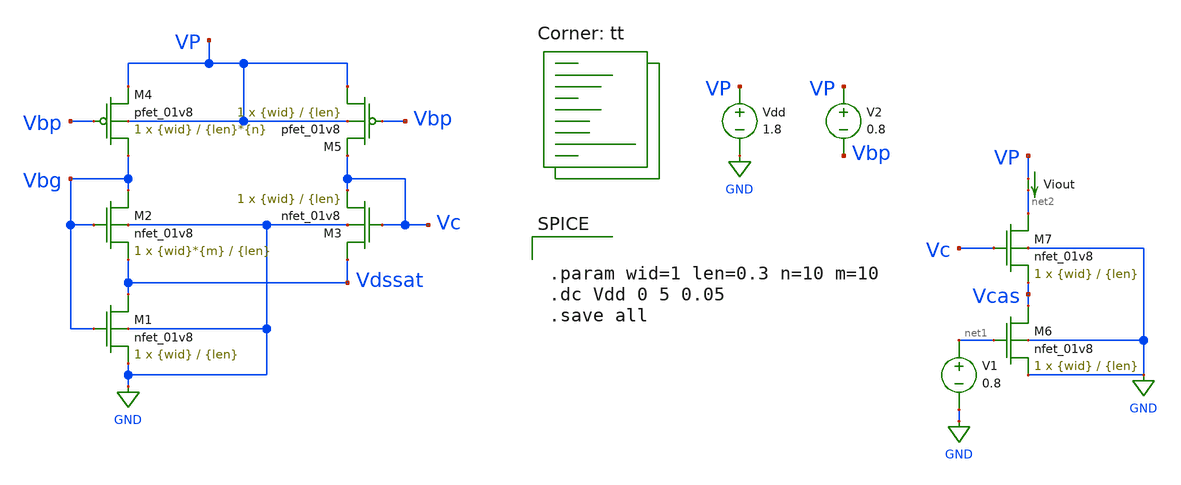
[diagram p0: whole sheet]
** sch_path: cbc.sch
**.subckt cbc
XM1 Vdssat Vbg GND GND sky130_fd_pr__nfet_01v8 L={len} W={wid} nf=1 ad='int((nf+1)/2) * W/nf * 0.29'
+ as='int((nf+2)/2) * W/nf * 0.29' pd='2*int((nf+1)/2) * (W/nf + 0.29)' ps='2*int((nf+2)/2) * (W/nf + 0.29)'
+ nrd='0.29 / W' nrs='0.29 / W' sa=0 sb=0 sd=0 mult=1 m=1
XM2 Vbg Vbg Vdssat GND sky130_fd_pr__nfet_01v8 L={len} W={wid}*{m} nf=1 ad='int((nf+1)/2) * W/nf * 0.29'
+ as='int((nf+2)/2) * W/nf * 0.29' pd='2*int((nf+1)/2) * (W/nf + 0.29)' ps='2*int((nf+2)/2) * (W/nf + 0.29)'
+ nrd='0.29 / W' nrs='0.29 / W' sa=0 sb=0 sd=0 mult=1 m=1
XM3 Vdssat Vc Vc GND sky130_fd_pr__nfet_01v8 L={len} W={wid} nf=1 ad='int((nf+1)/2) * W/nf * 0.29' as='int((nf+2)/2) * W/nf * 0.29'
+ pd='2*int((nf+1)/2) * (W/nf + 0.29)' ps='2*int((nf+2)/2) * (W/nf + 0.29)' nrd='0.29 / W' nrs='0.29 / W'
+ sa=0 sb=0 sd=0 mult=1 m=1
XM4 Vbg Vbp VP VP sky130_fd_pr__pfet_01v8 L={len}*{n} W={wid} nf=1 ad='int((nf+1)/2) * W/nf * 0.29' as='int((nf+2)/2) * W/nf * 0.29'
+ pd='2*int((nf+1)/2) * (W/nf + 0.29)' ps='2*int((nf+2)/2) * (W/nf + 0.29)' nrd='0.29 / W' nrs='0.29 / W'
+ sa=0 sb=0 sd=0 mult=1 m=1
XM5 VP Vbp Vc VP sky130_fd_pr__pfet_01v8 L={len} W={wid} nf=1 ad='int((nf+1)/2) * W/nf * 0.29' as='int((nf+2)/2) * W/nf * 0.29'
+ pd='2*int((nf+1)/2) * (W/nf + 0.29)' ps='2*int((nf+2)/2) * (W/nf + 0.29)' nrd='0.29 / W' nrs='0.29 / W'
+ sa=0 sb=0 sd=0 mult=1 m=1
Vdd VP GND 1.8
V2 VP Vbp 0.8
XM6 Vcas net1 GND GND sky130_fd_pr__nfet_01v8 L={len} W={wid} nf=1 ad='int((nf+1)/2) * W/nf * 0.29' as='int((nf+2)/2) * W/nf * 0.29'
+ pd='2*int((nf+1)/2) * (W/nf + 0.29)' ps='2*int((nf+2)/2) * (W/nf + 0.29)' nrd='0.29 / W' nrs='0.29 / W'
+ sa=0 sb=0 sd=0 mult=1 m=1
XM7 net2 Vc Vcas GND sky130_fd_pr__nfet_01v8 L={len} W={wid} nf=1 ad='int((nf+1)/2) * W/nf * 0.29' as='int((nf+2)/2) * W/nf * 0.29'
+ pd='2*int((nf+1)/2) * (W/nf + 0.29)' ps='2*int((nf+2)/2) * (W/nf + 0.29)' nrd='0.29 / W' nrs='0.29 / W'
+ sa=0 sb=0 sd=0 mult=1 m=1
V1 net1 GND 0.8
Viout VP net2 0
.save i(viout)
**** begin user architecture code


.param wid=1 len=0.3 n=10 m=10
.dc Vdd 0 5 0.05
.save all


.lib $::SKYWATER_MODELS/sky130.lib.spice tt
**** end user architecture code
**.ends
.GLOBAL GND
.end
